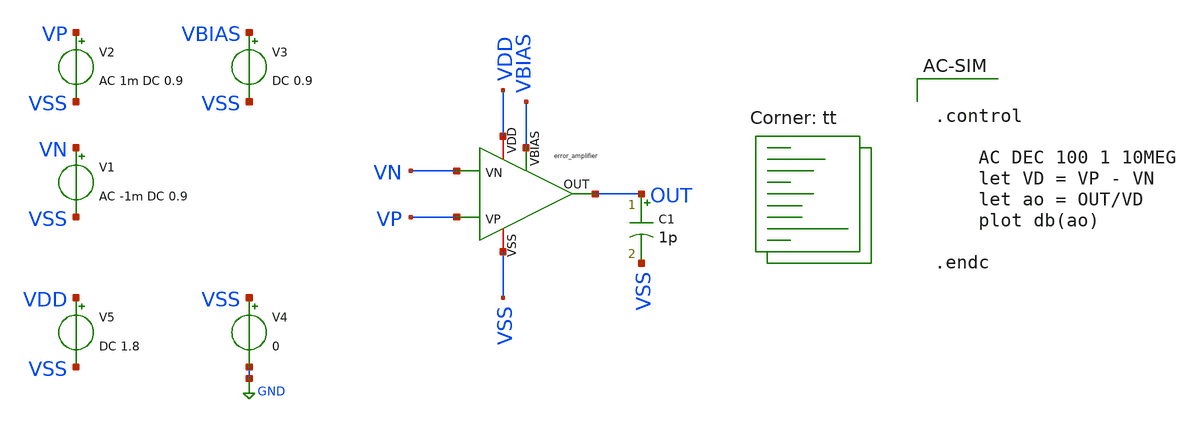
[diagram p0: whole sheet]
** sch_path: LDO_UVLO_Design/testbench/tb_error-amplifier/open-loop-gain.sch
**.subckt open-loop-gain
x1 VDD VBIAS VP VN OUT VSS error_amplifier
V1 VN VSS AC -1m DC 0.9
V2 VP VSS AC 1m DC 0.9
V3 VBIAS VSS DC 0.9
V4 VSS GND 0
V5 VDD VSS DC 1.8
C1 OUT VSS 1p m=1
**** begin user architecture code
.lib $::SKYWATER_MODELS/sky130.lib.spice tt


.control

	AC DEC 100 1 10MEG
	let VD = VP - VN
	let ao = OUT/VD
	plot db(ao)

.endc


**** end user architecture code
**.ends

* expanding   symbol:  ldo-sky130A-its/LDO_UVLO_Design/schematics/error_amplifier.sym # of pins=6
** sym_path: LDO_UVLO_Design/schematics/error_amplifier.sym
** sch_path: LDO_UVLO_Design/schematics/error_amplifier.sch
.subckt error_amplifier VDD VBIAS VP VN OUT VSS
*.iopin VDD
*.iopin VSS
*.ipin VBIAS
*.ipin VP
*.ipin VN
*.opin OUT
XM1 net2 net2 VSS VSS sky130_fd_pr__nfet_01v8 L=1.5 W=12 nf=1 ad='int((nf+1)/2) * W/nf * 0.29' as='int((nf+2)/2) * W/nf * 0.29'
+ pd='2*int((nf+1)/2) * (W/nf + 0.29)' ps='2*int((nf+2)/2) * (W/nf + 0.29)' nrd='0.29 / W' nrs='0.29 / W'
+ sa=0 sb=0 sd=0 mult=1 m=1
XM2 net1 net1 VSS VSS sky130_fd_pr__nfet_01v8 L=1.5 W=12 nf=1 ad='int((nf+1)/2) * W/nf * 0.29' as='int((nf+2)/2) * W/nf * 0.29'
+ pd='2*int((nf+1)/2) * (W/nf + 0.29)' ps='2*int((nf+2)/2) * (W/nf + 0.29)' nrd='0.29 / W' nrs='0.29 / W'
+ sa=0 sb=0 sd=0 mult=1 m=1
XM3 net2 VP net4 VDD sky130_fd_pr__pfet_01v8 L=1.5 W=12 nf=1 ad='int((nf+1)/2) * W/nf * 0.29' as='int((nf+2)/2) * W/nf * 0.29'
+ pd='2*int((nf+1)/2) * (W/nf + 0.29)' ps='2*int((nf+2)/2) * (W/nf + 0.29)' nrd='0.29 / W' nrs='0.29 / W'
+ sa=0 sb=0 sd=0 mult=1 m=1
XM4 net1 VN net4 VDD sky130_fd_pr__pfet_01v8 L=1.5 W=12 nf=1 ad='int((nf+1)/2) * W/nf * 0.29' as='int((nf+2)/2) * W/nf * 0.29'
+ pd='2*int((nf+1)/2) * (W/nf + 0.29)' ps='2*int((nf+2)/2) * (W/nf + 0.29)' nrd='0.29 / W' nrs='0.29 / W'
+ sa=0 sb=0 sd=0 mult=1 m=1
XM7 net3 net1 VSS VSS sky130_fd_pr__nfet_01v8 L=1.5 W=12 nf=1 ad='int((nf+1)/2) * W/nf * 0.29' as='int((nf+2)/2) * W/nf * 0.29'
+ pd='2*int((nf+1)/2) * (W/nf + 0.29)' ps='2*int((nf+2)/2) * (W/nf + 0.29)' nrd='0.29 / W' nrs='0.29 / W'
+ sa=0 sb=0 sd=0 mult=1 m=1
XM8 OUT net2 VSS VSS sky130_fd_pr__nfet_01v8 L=1.5 W=12 nf=1 ad='int((nf+1)/2) * W/nf * 0.29' as='int((nf+2)/2) * W/nf * 0.29'
+ pd='2*int((nf+1)/2) * (W/nf + 0.29)' ps='2*int((nf+2)/2) * (W/nf + 0.29)' nrd='0.29 / W' nrs='0.29 / W'
+ sa=0 sb=0 sd=0 mult=1 m=1
XM9 net3 net3 VDD VDD sky130_fd_pr__pfet_01v8 L=1.5 W=12 nf=1 ad='int((nf+1)/2) * W/nf * 0.29' as='int((nf+2)/2) * W/nf * 0.29'
+ pd='2*int((nf+1)/2) * (W/nf + 0.29)' ps='2*int((nf+2)/2) * (W/nf + 0.29)' nrd='0.29 / W' nrs='0.29 / W'
+ sa=0 sb=0 sd=0 mult=1 m=1
XM10 OUT net3 VDD VDD sky130_fd_pr__pfet_01v8 L=1.5 W=12 nf=1 ad='int((nf+1)/2) * W/nf * 0.29' as='int((nf+2)/2) * W/nf * 0.29'
+ pd='2*int((nf+1)/2) * (W/nf + 0.29)' ps='2*int((nf+2)/2) * (W/nf + 0.29)' nrd='0.29 / W' nrs='0.29 / W'
+ sa=0 sb=0 sd=0 mult=1 m=1
XM11 net4 VBIAS VDD VDD sky130_fd_pr__pfet_01v8 L=1.5 W=12 nf=1 ad='int((nf+1)/2) * W/nf * 0.29' as='int((nf+2)/2) * W/nf * 0.29'
+ pd='2*int((nf+1)/2) * (W/nf + 0.29)' ps='2*int((nf+2)/2) * (W/nf + 0.29)' nrd='0.29 / W' nrs='0.29 / W'
+ sa=0 sb=0 sd=0 mult=1 m=1
.ends

.GLOBAL GND
.end
